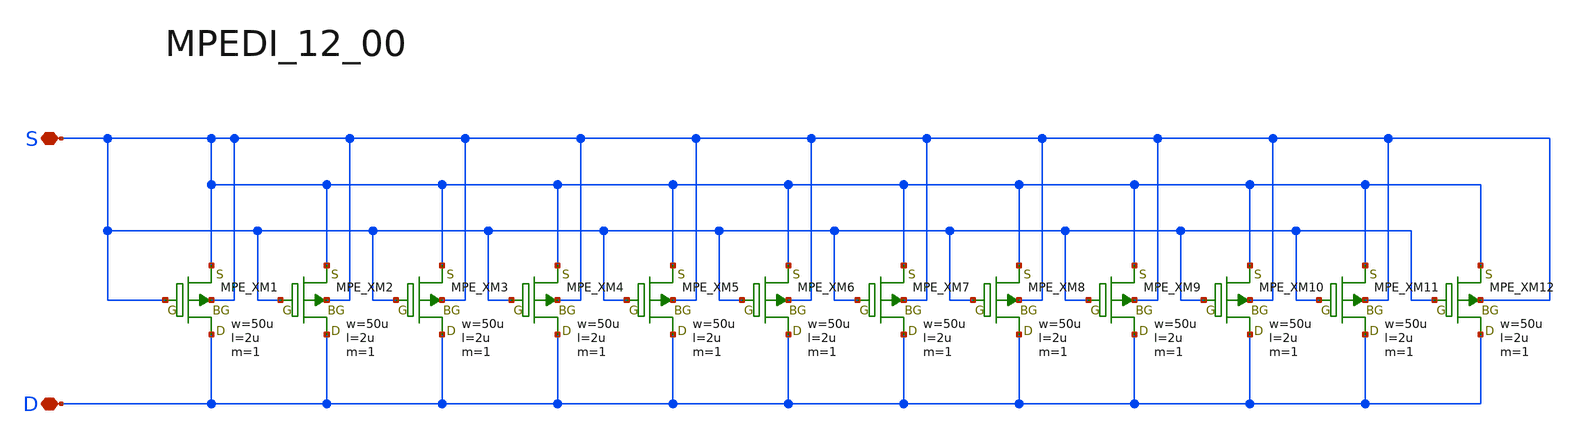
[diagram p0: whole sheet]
** sch_path: libs.tech/xschem/TR-1um_2_ESD/MPEDI_12_00.sch
**.subckt MPEDI_12_00 S D
*.iopin S
*.iopin D
XXM1 D S S S MPE w=50u l=2u as=0 ad=0 ps=0 pd=0 nrd=0 nrs=0 m=1
XXM2 D S S S MPE w=50u l=2u as=0 ad=0 ps=0 pd=0 nrd=0 nrs=0 m=1
XXM3 D S S S MPE w=50u l=2u as=0 ad=0 ps=0 pd=0 nrd=0 nrs=0 m=1
XXM4 D S S S MPE w=50u l=2u as=0 ad=0 ps=0 pd=0 nrd=0 nrs=0 m=1
XXM5 D S S S MPE w=50u l=2u as=0 ad=0 ps=0 pd=0 nrd=0 nrs=0 m=1
XXM6 D S S S MPE w=50u l=2u as=0 ad=0 ps=0 pd=0 nrd=0 nrs=0 m=1
XXM7 D S S S MPE w=50u l=2u as=0 ad=0 ps=0 pd=0 nrd=0 nrs=0 m=1
XXM8 D S S S MPE w=50u l=2u as=0 ad=0 ps=0 pd=0 nrd=0 nrs=0 m=1
XXM9 D S S S MPE w=50u l=2u as=0 ad=0 ps=0 pd=0 nrd=0 nrs=0 m=1
XXM10 D S S S MPE w=50u l=2u as=0 ad=0 ps=0 pd=0 nrd=0 nrs=0 m=1
XXM11 D S S S MPE w=50u l=2u as=0 ad=0 ps=0 pd=0 nrd=0 nrs=0 m=1
XXM12 D S S S MPE w=50u l=2u as=0 ad=0 ps=0 pd=0 nrd=0 nrs=0 m=1
**.ends
.end
